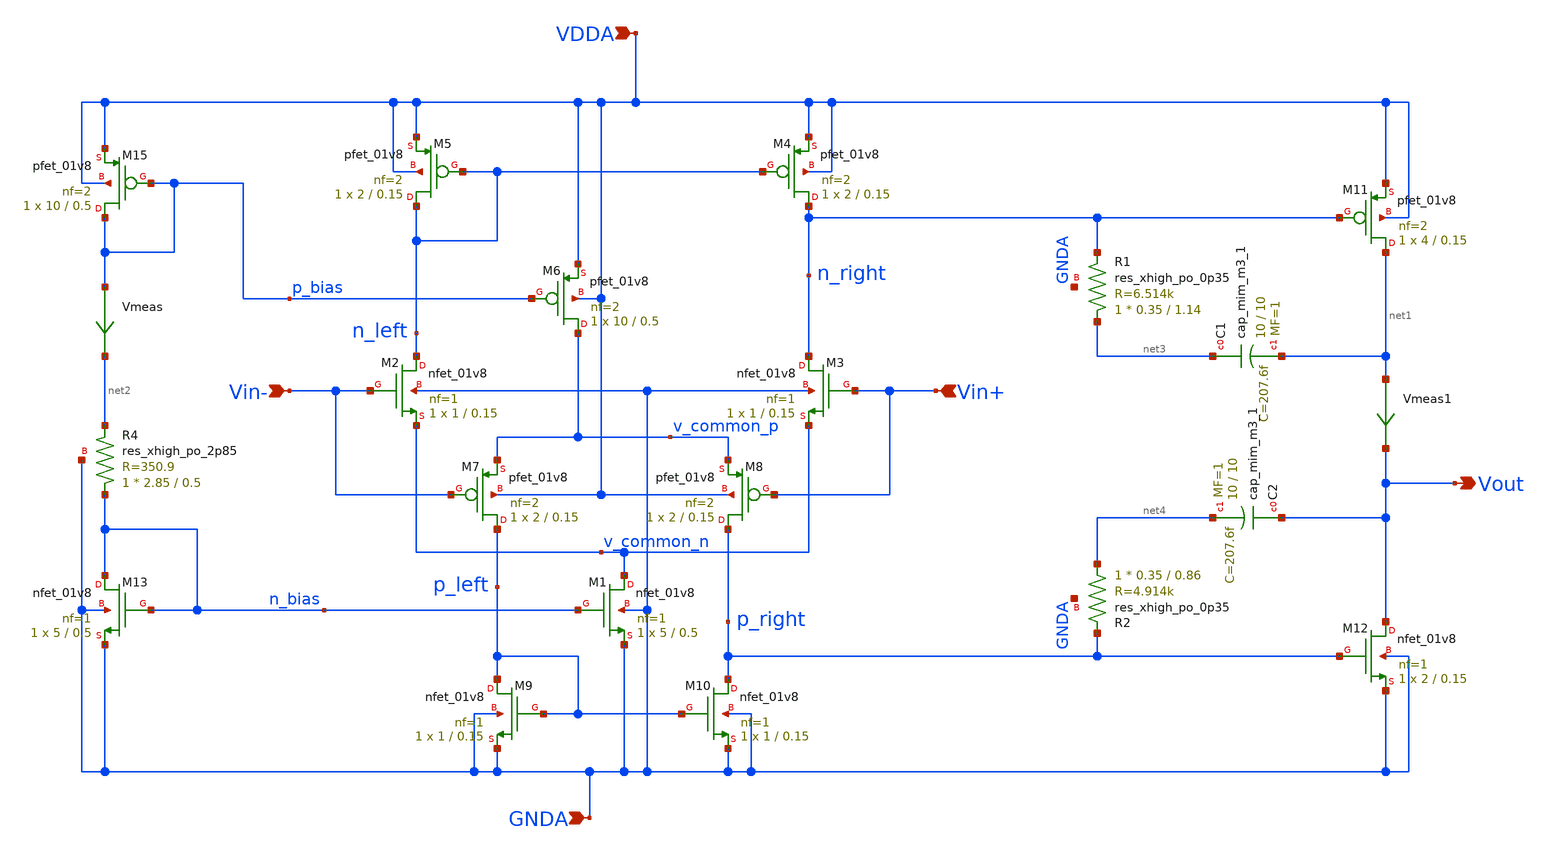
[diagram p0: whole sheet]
** sch_path: projects/pll/charge_pump/xschem_ngspice/rail_to_rail_opamp6.sch
**.subckt rail_to_rail_opamp6 Vout Vin+ Vin- VDDA GNDA
*.opin Vout
*.ipin Vin+
*.ipin Vin-
*.ipin VDDA
*.ipin GNDA
XM2 n_left Vin- v_common_n GNDA sky130_fd_pr__nfet_01v8 L=0.15 W=1 nf=1 ad='int((nf+1)/2) * W/nf * 0.29'
+ as='int((nf+2)/2) * W/nf * 0.29' pd='2*int((nf+1)/2) * (W/nf + 0.29)' ps='2*int((nf+2)/2) * (W/nf + 0.29)'
+ nrd='0.29 / W' nrs='0.29 / W' sa=0 sb=0 sd=0 mult=1 m=1
XM3 n_right Vin+ v_common_n GNDA sky130_fd_pr__nfet_01v8 L=0.15 W=1 nf=1 ad='int((nf+1)/2) * W/nf * 0.29'
+ as='int((nf+2)/2) * W/nf * 0.29' pd='2*int((nf+1)/2) * (W/nf + 0.29)' ps='2*int((nf+2)/2) * (W/nf + 0.29)'
+ nrd='0.29 / W' nrs='0.29 / W' sa=0 sb=0 sd=0 mult=1 m=1
XM5 n_left n_left VDDA VDDA sky130_fd_pr__pfet_01v8 L=0.15 W=2 nf=2 ad='int((nf+1)/2) * W/nf * 0.29'
+ as='int((nf+2)/2) * W/nf * 0.29' pd='2*int((nf+1)/2) * (W/nf + 0.29)' ps='2*int((nf+2)/2) * (W/nf + 0.29)'
+ nrd='0.29 / W' nrs='0.29 / W' sa=0 sb=0 sd=0 mult=1 m=1
XM4 n_right n_left VDDA VDDA sky130_fd_pr__pfet_01v8 L=0.15 W=2 nf=2 ad='int((nf+1)/2) * W/nf * 0.29'
+ as='int((nf+2)/2) * W/nf * 0.29' pd='2*int((nf+1)/2) * (W/nf + 0.29)' ps='2*int((nf+2)/2) * (W/nf + 0.29)'
+ nrd='0.29 / W' nrs='0.29 / W' sa=0 sb=0 sd=0 mult=1 m=1
XM6 v_common_p p_bias VDDA VDDA sky130_fd_pr__pfet_01v8 L=0.5 W=10 nf=2 ad='int((nf+1)/2) * W/nf * 0.29'
+ as='int((nf+2)/2) * W/nf * 0.29' pd='2*int((nf+1)/2) * (W/nf + 0.29)' ps='2*int((nf+2)/2) * (W/nf + 0.29)'
+ nrd='0.29 / W' nrs='0.29 / W' sa=0 sb=0 sd=0 mult=1 m=1
XM7 p_left Vin- v_common_p VDDA sky130_fd_pr__pfet_01v8 L=0.15 W=2 nf=2 ad='int((nf+1)/2) * W/nf * 0.29'
+ as='int((nf+2)/2) * W/nf * 0.29' pd='2*int((nf+1)/2) * (W/nf + 0.29)' ps='2*int((nf+2)/2) * (W/nf + 0.29)'
+ nrd='0.29 / W' nrs='0.29 / W' sa=0 sb=0 sd=0 mult=1 m=1
XM8 p_right Vin+ v_common_p VDDA sky130_fd_pr__pfet_01v8 L=0.15 W=2 nf=2 ad='int((nf+1)/2) * W/nf * 0.29'
+ as='int((nf+2)/2) * W/nf * 0.29' pd='2*int((nf+1)/2) * (W/nf + 0.29)' ps='2*int((nf+2)/2) * (W/nf + 0.29)'
+ nrd='0.29 / W' nrs='0.29 / W' sa=0 sb=0 sd=0 mult=1 m=1
XM9 p_left p_left GNDA GNDA sky130_fd_pr__nfet_01v8 L=0.15 W=1 nf=1 ad='int((nf+1)/2) * W/nf * 0.29'
+ as='int((nf+2)/2) * W/nf * 0.29' pd='2*int((nf+1)/2) * (W/nf + 0.29)' ps='2*int((nf+2)/2) * (W/nf + 0.29)'
+ nrd='0.29 / W' nrs='0.29 / W' sa=0 sb=0 sd=0 mult=1 m=1
XM10 p_right p_left GNDA GNDA sky130_fd_pr__nfet_01v8 L=0.15 W=1 nf=1 ad='int((nf+1)/2) * W/nf * 0.29'
+ as='int((nf+2)/2) * W/nf * 0.29' pd='2*int((nf+1)/2) * (W/nf + 0.29)' ps='2*int((nf+2)/2) * (W/nf + 0.29)'
+ nrd='0.29 / W' nrs='0.29 / W' sa=0 sb=0 sd=0 mult=1 m=1
XM1 v_common_n n_bias GNDA GNDA sky130_fd_pr__nfet_01v8 L=0.5 W=5 nf=1 ad='int((nf+1)/2) * W/nf * 0.29'
+ as='int((nf+2)/2) * W/nf * 0.29' pd='2*int((nf+1)/2) * (W/nf + 0.29)' ps='2*int((nf+2)/2) * (W/nf + 0.29)'
+ nrd='0.29 / W' nrs='0.29 / W' sa=0 sb=0 sd=0 mult=1 m=1
XM11 net1 n_right VDDA VDDA sky130_fd_pr__pfet_01v8 L=0.15 W=4 nf=2 ad='int((nf+1)/2) * W/nf * 0.29'
+ as='int((nf+2)/2) * W/nf * 0.29' pd='2*int((nf+1)/2) * (W/nf + 0.29)' ps='2*int((nf+2)/2) * (W/nf + 0.29)'
+ nrd='0.29 / W' nrs='0.29 / W' sa=0 sb=0 sd=0 mult=1 m=1
XM12 Vout p_right GNDA GNDA sky130_fd_pr__nfet_01v8 L=0.15 W=2 nf=1 ad='int((nf+1)/2) * W/nf * 0.29'
+ as='int((nf+2)/2) * W/nf * 0.29' pd='2*int((nf+1)/2) * (W/nf + 0.29)' ps='2*int((nf+2)/2) * (W/nf + 0.29)'
+ nrd='0.29 / W' nrs='0.29 / W' sa=0 sb=0 sd=0 mult=1 m=1
XM13 n_bias n_bias GNDA GNDA sky130_fd_pr__nfet_01v8 L=0.5 W=5 nf=1 ad='int((nf+1)/2) * W/nf * 0.29'
+ as='int((nf+2)/2) * W/nf * 0.29' pd='2*int((nf+1)/2) * (W/nf + 0.29)' ps='2*int((nf+2)/2) * (W/nf + 0.29)'
+ nrd='0.29 / W' nrs='0.29 / W' sa=0 sb=0 sd=0 mult=1 m=1
XM15 p_bias p_bias VDDA VDDA sky130_fd_pr__pfet_01v8 L=0.5 W=10 nf=2 ad='int((nf+1)/2) * W/nf * 0.29'
+ as='int((nf+2)/2) * W/nf * 0.29' pd='2*int((nf+1)/2) * (W/nf + 0.29)' ps='2*int((nf+2)/2) * (W/nf + 0.29)'
+ nrd='0.29 / W' nrs='0.29 / W' sa=0 sb=0 sd=0 mult=1 m=1
Vmeas p_bias net2 0
.save i(vmeas)
XC1 net3 net1 sky130_fd_pr__cap_mim_m3_1 W=10 L=10 MF=1 m=1
XC2 Vout net4 sky130_fd_pr__cap_mim_m3_1 W=10 L=10 MF=1 m=1
XR1 net3 n_right GNDA sky130_fd_pr__res_xhigh_po_0p35 L=1.14 mult=1 m=1
XR2 net4 p_right GNDA sky130_fd_pr__res_xhigh_po_0p35 L=0.86 mult=1 m=1
Vmeas1 net1 Vout 0
.save i(vmeas1)
XR4 n_bias net2 GNDA sky130_fd_pr__res_xhigh_po_2p85 L=0.5 mult=1 m=1
**.ends
.end
